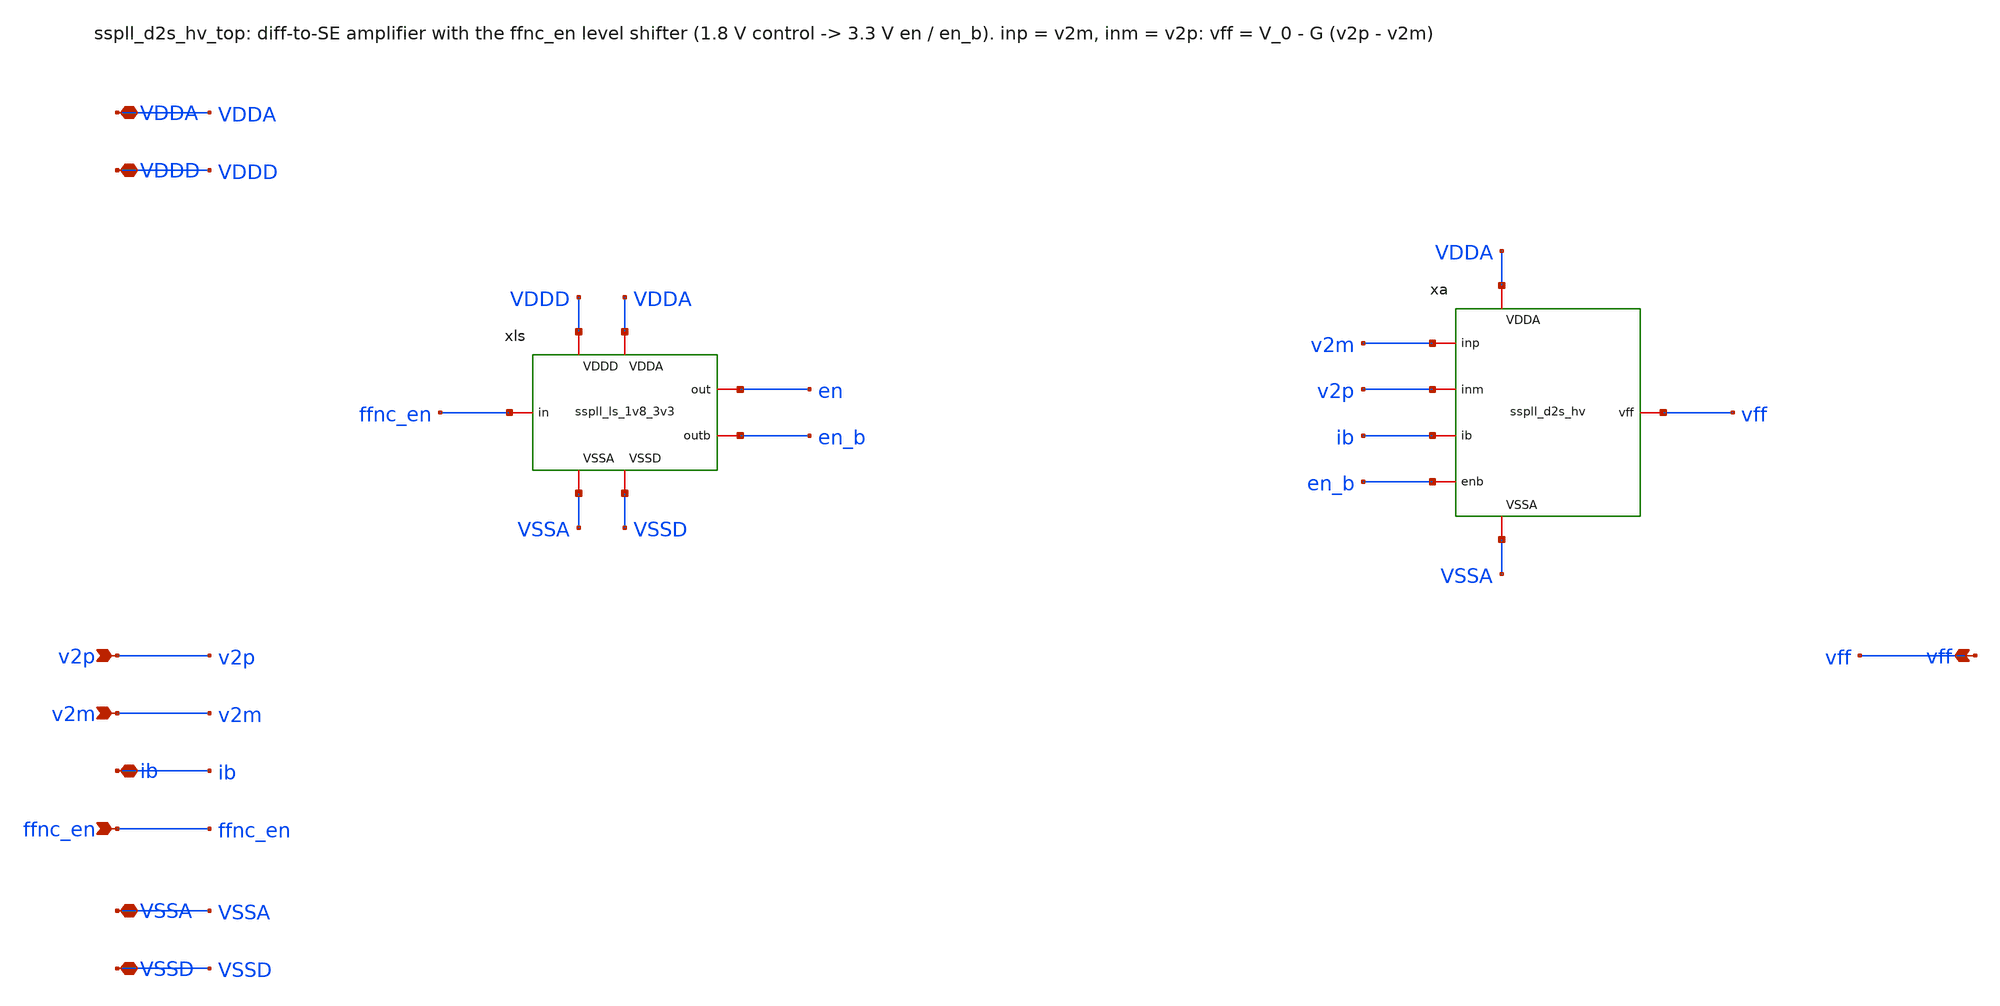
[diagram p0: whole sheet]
** sch_path: xschem/d2s_hv/sspll_d2s_hv_top.sch
**.subckt sspll_d2s_hv_top v2p v2m ib ffnc_en vff VDDA VDDD VSSA VSSD
*.ipin v2p
*.ipin v2m
*.iopin ib
*.ipin ffnc_en
*.opin vff
*.iopin VDDA
*.iopin VDDD
*.iopin VSSA
*.iopin VSSD
xls ffnc_en en en_b VDDD VDDA VSSA VSSD sspll_ls_1v8_3v3
xa v2m v2p ib en_b vff VDDA VSSA sspll_d2s_hv
**.ends
.end
